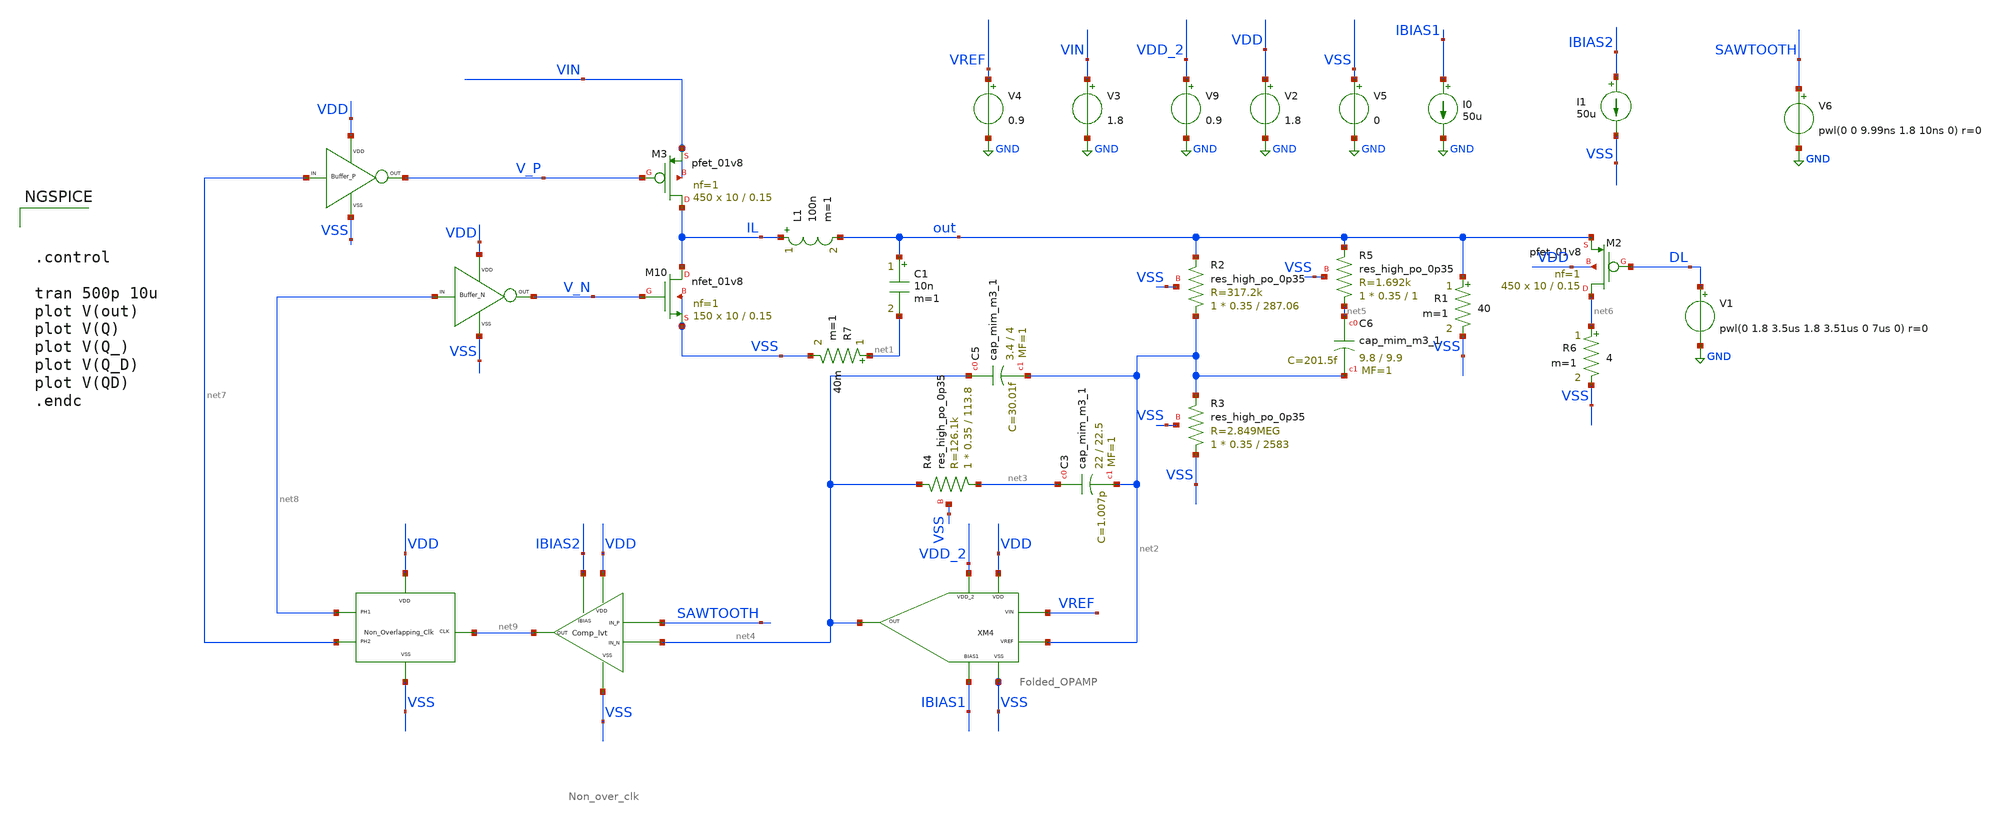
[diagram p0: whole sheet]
** sch_path: xschem/DC_DC_Converter_xschem/OTHERS/DC_DC_Converter_JV10/TOP_LEVEL/closed_loop_jd_sep.sch
**.subckt closed_loop_jd_sep
XM3 IL V_P VIN VIN sky130_fd_pr__pfet_01v8 L=0.15 W=10 nf=1 ad='int((nf+1)/2) * W/nf * 0.29' as='int((nf+2)/2) * W/nf * 0.29'
+ pd='2*int((nf+1)/2) * (W/nf + 0.29)' ps='2*int((nf+2)/2) * (W/nf + 0.29)' nrd='0.29 / W' nrs='0.29 / W'
+ sa=0 sb=0 sd=0 mult=450 m=450
L1 IL out 100n m=1
C1 out net1 10n m=1
V3 VIN GND 1.8
I0 IBIAS1 GND 50u
V9 VDD_2 GND 0.9
V2 VDD GND 1.8
V5 VSS GND 0
V4 VREF GND 0.9
I1 IBIAS2 VSS 50u
V6 SAWTOOTH GND pwl(0 0 9.99ns 1.8 10ns 0) r=0
XM2 net6 DL out VDD sky130_fd_pr__pfet_01v8 L=0.15 W=10 nf=1 ad='int((nf+1)/2) * W/nf * 0.29' as='int((nf+2)/2) * W/nf * 0.29'
+ pd='2*int((nf+1)/2) * (W/nf + 0.29)' ps='2*int((nf+2)/2) * (W/nf + 0.29)' nrd='0.29 / W' nrs='0.29 / W'
+ sa=0 sb=0 sd=0 mult=450 m=450
V1 DL GND pwl(0 1.8 3.5us 1.8 3.51us 0 7us 0) r=0
X1 net7 V_P VDD VSS BUFFER_P
X2 net8 V_N VDD VSS BUFFER_N
XM3 VDD net9 net8 VSS net7 Non_over_clk
XM4 VDD VSS VDD_2 IBIAS1 net4 VREF net2 Folded_OPAMP
XC5 net4 net2 sky130_fd_pr__cap_mim_m3_1 W=3.4 L=4 MF=1 m=1
XC3 net3 net2 sky130_fd_pr__cap_mim_m3_1 W=22 L=22.5 MF=1 m=1
XC6 net5 net2 sky130_fd_pr__cap_mim_m3_1 W=9.8 L=9.9 MF=1 m=1
XM10 IL V_N VSS VSS sky130_fd_pr__nfet_01v8 L=0.15 W=10 nf=1 ad='int((nf+1)/2) * W/nf * 0.29' as='int((nf+2)/2) * W/nf * 0.29'
+ pd='2*int((nf+1)/2) * (W/nf + 0.29)' ps='2*int((nf+2)/2) * (W/nf + 0.29)' nrd='0.29 / W' nrs='0.29 / W'
+ sa=0 sb=0 sd=0 mult=150 m=150
XR4 net3 net4 VSS sky130_fd_pr__res_high_po_0p35 L=113.8 mult=1 m=1
XR5 net5 out VSS sky130_fd_pr__res_high_po_0p35 L=1 mult=1 m=1
XR2 net2 out VSS sky130_fd_pr__res_high_po_0p35 L=287.06 mult=1 m=1
XR3 VSS net2 VSS sky130_fd_pr__res_high_po_0p35 L=2583 mult=1 m=1
R7 net1 VSS 40m m=1
R1 out VSS 40 m=1
R6 net6 VSS 4 m=1
XM2 IBIAS2 VDD SAWTOOTH net4 VSS net9 Comp_lvt
**** begin user architecture code

** opencircuitdesign pdks install
.lib $::SKYWATER_MODELS/sky130.lib.spice tt





.control

tran 500p 10u
plot V(out)
plot V(Q)
plot V(Q_)
plot V(Q_D)
plot V(QD)
.endc


**** end user architecture code
**.ends
.GLOBAL GND
.end
